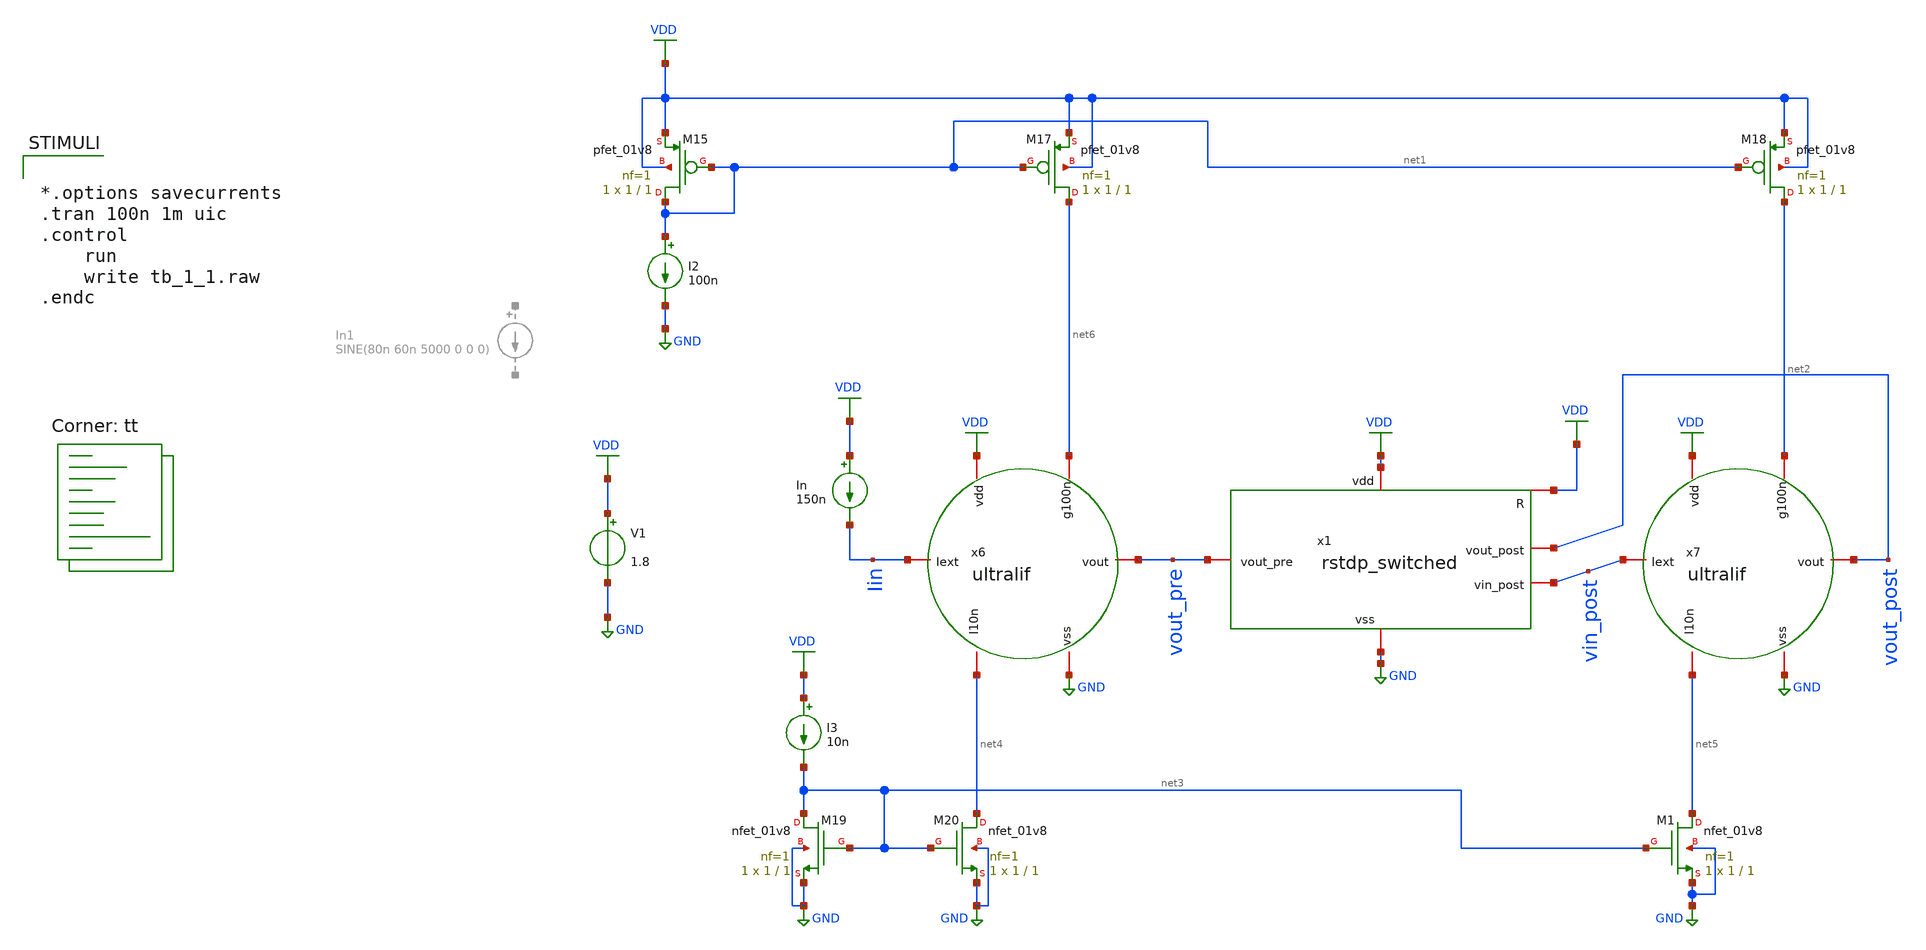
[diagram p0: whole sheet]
** sch_path: tb_1_1.sch
**.subckt tb_1_1
V1 VDD GND 1.8
x6 VDD Iin vout_pre net4 GND net6 ultralif
x7 VDD vin_post vout_post net5 GND net2 ultralif
XM15 net1 net1 VDD VDD sky130_fd_pr__pfet_01v8 L=1 W=1 nf=1 ad='int((nf+1)/2) * W/nf * 0.29' as='int((nf+2)/2) * W/nf * 0.29'
+ pd='2*int((nf+1)/2) * (W/nf + 0.29)' ps='2*int((nf+2)/2) * (W/nf + 0.29)' nrd='0.29 / W' nrs='0.29 / W'
+ sa=0 sb=0 sd=0 mult=1 m=1
XM17 net6 net1 VDD VDD sky130_fd_pr__pfet_01v8 L=1 W=1 nf=1 ad='int((nf+1)/2) * W/nf * 0.29' as='int((nf+2)/2) * W/nf * 0.29'
+ pd='2*int((nf+1)/2) * (W/nf + 0.29)' ps='2*int((nf+2)/2) * (W/nf + 0.29)' nrd='0.29 / W' nrs='0.29 / W'
+ sa=0 sb=0 sd=0 mult=1 m=1
I2 net1 GND 100n
XM18 net2 net1 VDD VDD sky130_fd_pr__pfet_01v8 L=1 W=1 nf=1 ad='int((nf+1)/2) * W/nf * 0.29' as='int((nf+2)/2) * W/nf * 0.29'
+ pd='2*int((nf+1)/2) * (W/nf + 0.29)' ps='2*int((nf+2)/2) * (W/nf + 0.29)' nrd='0.29 / W' nrs='0.29 / W'
+ sa=0 sb=0 sd=0 mult=1 m=1
XM19 net3 net3 GND GND sky130_fd_pr__nfet_01v8 L=1 W=1 nf=1 ad='int((nf+1)/2) * W/nf * 0.29' as='int((nf+2)/2) * W/nf * 0.29'
+ pd='2*int((nf+1)/2) * (W/nf + 0.29)' ps='2*int((nf+2)/2) * (W/nf + 0.29)' nrd='0.29 / W' nrs='0.29 / W'
+ sa=0 sb=0 sd=0 mult=1 m=1
I3 VDD net3 10n
XM20 net4 net3 GND GND sky130_fd_pr__nfet_01v8 L=1 W=1 nf=1 ad='int((nf+1)/2) * W/nf * 0.29' as='int((nf+2)/2) * W/nf * 0.29'
+ pd='2*int((nf+1)/2) * (W/nf + 0.29)' ps='2*int((nf+2)/2) * (W/nf + 0.29)' nrd='0.29 / W' nrs='0.29 / W'
+ sa=0 sb=0 sd=0 mult=1 m=1
XM1 net5 net3 GND GND sky130_fd_pr__nfet_01v8 L=1 W=1 nf=1 ad='int((nf+1)/2) * W/nf * 0.29' as='int((nf+2)/2) * W/nf * 0.29'
+ pd='2*int((nf+1)/2) * (W/nf + 0.29)' ps='2*int((nf+2)/2) * (W/nf + 0.29)' nrd='0.29 / W' nrs='0.29 / W'
+ sa=0 sb=0 sd=0 mult=1 m=1
x1 VDD VDD GND vout_pre vout_post vin_post rstdp_switched
In VDD Iin 150n
**** begin user architecture code
.lib $::SKYWATER_MODELS/sky130.lib.spice tt

** opencircuitdesign pdks install
.inc $::SKYWATER_MODELS/rram_v0.spice

**** end user architecture code
**.ends
.GLOBAL VDD
.GLOBAL GND
**** begin user architecture code


*.options savecurrents
.tran 100n 1m uic
.control
	run
	write tb_1_1.raw
.endc


**** end user architecture code
.end
